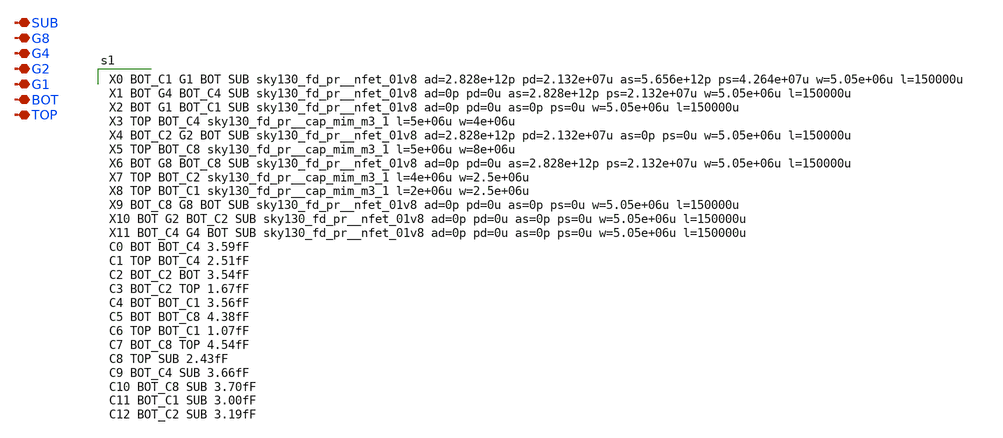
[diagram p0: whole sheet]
** sch_path: xschem/captuner_complete_1_r_PEX.sch
**.subckt captuner_complete_1_r_PEX SUB G8 G4 G2 G1 BOT TOP
*.iopin SUB
*.iopin G8
*.iopin G4
*.iopin G2
*.iopin G1
*.iopin BOT
*.iopin TOP
**** begin user architecture code

X0 BOT_C1 G1 BOT SUB sky130_fd_pr__nfet_01v8 ad=2.828e+12p pd=2.132e+07u as=5.656e+12p ps=4.264e+07u
+ w=5.05e+06u l=150000u
X1 BOT G4 BOT_C4 SUB sky130_fd_pr__nfet_01v8 ad=0p pd=0u as=2.828e+12p ps=2.132e+07u w=5.05e+06u
+ l=150000u
X2 BOT G1 BOT_C1 SUB sky130_fd_pr__nfet_01v8 ad=0p pd=0u as=0p ps=0u w=5.05e+06u l=150000u
X3 TOP BOT_C4 sky130_fd_pr__cap_mim_m3_1 l=5e+06u w=4e+06u
X4 BOT_C2 G2 BOT SUB sky130_fd_pr__nfet_01v8 ad=2.828e+12p pd=2.132e+07u as=0p ps=0u w=5.05e+06u
+ l=150000u
X5 TOP BOT_C8 sky130_fd_pr__cap_mim_m3_1 l=5e+06u w=8e+06u
X6 BOT G8 BOT_C8 SUB sky130_fd_pr__nfet_01v8 ad=0p pd=0u as=2.828e+12p ps=2.132e+07u w=5.05e+06u
+ l=150000u
X7 TOP BOT_C2 sky130_fd_pr__cap_mim_m3_1 l=4e+06u w=2.5e+06u
X8 TOP BOT_C1 sky130_fd_pr__cap_mim_m3_1 l=2e+06u w=2.5e+06u
X9 BOT_C8 G8 BOT SUB sky130_fd_pr__nfet_01v8 ad=0p pd=0u as=0p ps=0u w=5.05e+06u l=150000u
X10 BOT G2 BOT_C2 SUB sky130_fd_pr__nfet_01v8 ad=0p pd=0u as=0p ps=0u w=5.05e+06u l=150000u
X11 BOT_C4 G4 BOT SUB sky130_fd_pr__nfet_01v8 ad=0p pd=0u as=0p ps=0u w=5.05e+06u l=150000u
C0 BOT BOT_C4 3.59fF
C1 TOP BOT_C4 2.51fF
C2 BOT_C2 BOT 3.54fF
C3 BOT_C2 TOP 1.67fF
C4 BOT BOT_C1 3.56fF
C5 BOT BOT_C8 4.38fF
C6 TOP BOT_C1 1.07fF
C7 BOT_C8 TOP 4.54fF
C8 TOP SUB 2.43fF
C9 BOT_C4 SUB 3.66fF
C10 BOT_C8 SUB 3.70fF
C11 BOT_C1 SUB 3.00fF
C12 BOT_C2 SUB 3.19fF


**** end user architecture code
**.ends
.end
